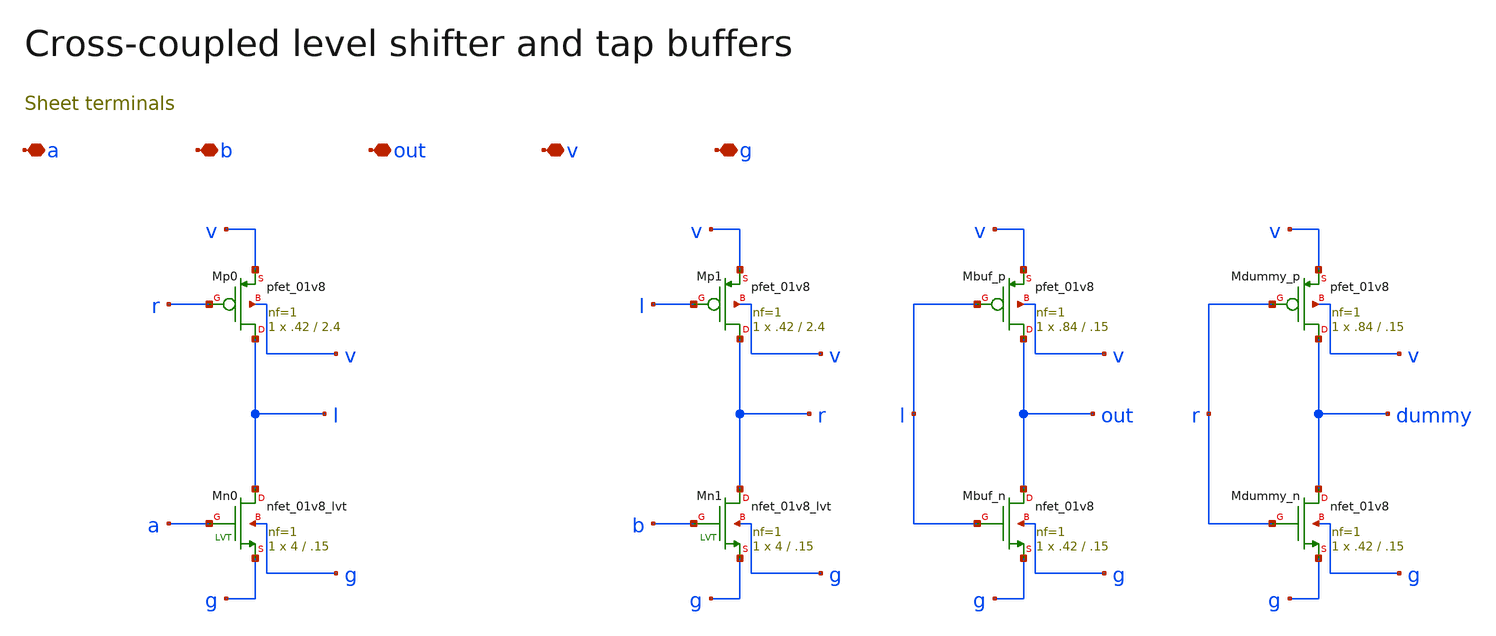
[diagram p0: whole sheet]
** sch_path: review/xschem/cvsl.sch
**.subckt cvsl a b out v g
*.iopin a
*.iopin b
*.iopin out
*.iopin v
*.iopin g
XMn0 l a g g sky130_fd_pr__nfet_01v8_lvt L=.15 W=4 nf=1 ad=1.16 as=1.16 pd=8.58 ps=8.58 nrd='0.29 / 4 '
+ nrs='0.29 / 4 ' sa=0 sb=0 sd=0 mult=1 m=1
XMn1 r b g g sky130_fd_pr__nfet_01v8_lvt L=.15 W=4 nf=1 ad=1.16 as=1.16 pd=8.58 ps=8.58 nrd='0.29 / 4 '
+ nrs='0.29 / 4 ' sa=0 sb=0 sd=0 mult=1 m=1
XMp0 l r v v sky130_fd_pr__pfet_01v8 L=2.4 W=.42 nf=1 ad=.122 as=.122 pd=1.42 ps=1.42 nrd='0.29 / W'
+ nrs='0.29 / W' sa=0 sb=0 sd=0 mult=1 m=1
XMp1 r l v v sky130_fd_pr__pfet_01v8 L=2.4 W=.42 nf=1 ad=.122 as=.122 pd=1.42 ps=1.42 nrd='0.29 / W'
+ nrs='0.29 / W' sa=0 sb=0 sd=0 mult=1 m=1
XMbuf_p out l v v sky130_fd_pr__pfet_01v8 L=.15 W=.84 nf=1 ad='int((nf+1)/2) * W/nf * 0.29' as='int((nf+2)/2) * W/nf * 0.29'
+ pd='2*int((nf+1)/2) * (W/nf + 0.29)' ps='2*int((nf+2)/2) * (W/nf + 0.29)' nrd='0.29 / W' nrs='0.29 / W'
+ sa=0 sb=0 sd=0 mult=1 m=1
XMbuf_n out l g g sky130_fd_pr__nfet_01v8 L=.15 W=.42 nf=1 ad='int((1 + 1)/2) * .42 / 1 * 0.29' as='int((1 + 2)/2) * .42 / 1 * 0.29'
+ pd='2*int((1 + 1)/2) * (.42 / 1 + 0.29)' ps='2*int((1 + 2)/2) * (.42 / 1 + 0.29)' nrd='0.29 / .42 ' nrs='0.29 / .42 '
+ sa=0 sb=0 sd=0 mult=1 m=1
XMdummy_p dummy r v v sky130_fd_pr__pfet_01v8 L=.15 W=.84 nf=1 ad='int((nf+1)/2) * W/nf * 0.29' as='int((nf+2)/2) * W/nf * 0.29'
+ pd='2*int((nf+1)/2) * (W/nf + 0.29)' ps='2*int((nf+2)/2) * (W/nf + 0.29)' nrd='0.29 / W' nrs='0.29 / W'
+ sa=0 sb=0 sd=0 mult=1 m=1
XMdummy_n dummy r g g sky130_fd_pr__nfet_01v8 L=.15 W=.42 nf=1 ad='int((1 + 1)/2) * .42 / 1 * 0.29' as='int((1 + 2)/2) * .42 / 1 * 0.29'
+ pd='2*int((1 + 1)/2) * (.42 / 1 + 0.29)' ps='2*int((1 + 2)/2) * (.42 / 1 + 0.29)' nrd='0.29 / .42 ' nrs='0.29 / .42 '
+ sa=0 sb=0 sd=0 mult=1 m=1
**.ends
.end
